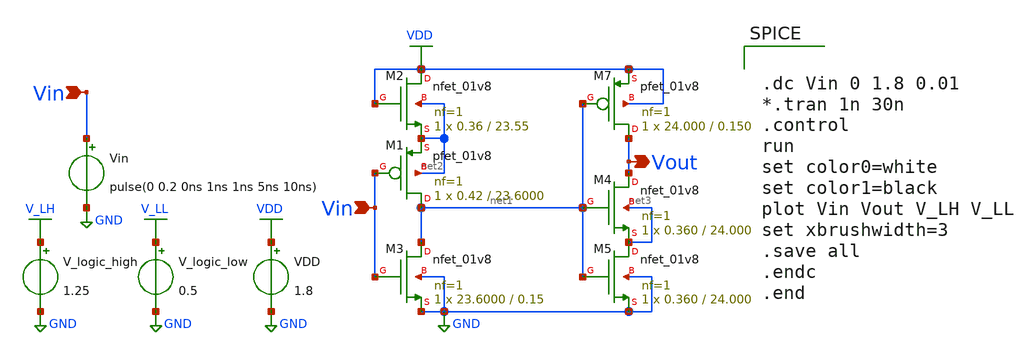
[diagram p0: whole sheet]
** sch_path: xschem/Vth_sch/th02.sch
**.subckt th02 Vin Vin Vout
*.ipin Vin
*.ipin Vin
*.opin Vout
VDD VDD GND 1.8
Vin Vin GND pulse(0 0.2 0ns 1ns 1ns 5ns 10ns)
V_logic_high V_LH GND 1.25
V_logic_low V_LL GND 0.5
XM7 Vout net1 VDD VDD sky130_fd_pr__pfet_01v8 L=0.150 W=24.000 nf=1 ad='int((nf+1)/2) * W/nf * 0.29'
+ as='int((nf+2)/2) * W/nf * 0.29' pd='2*int((nf+1)/2) * (W/nf + 0.29)' ps='2*int((nf+2)/2) * (W/nf + 0.29)'
+ nrd='0.29 / W' nrs='0.29 / W' sa=0 sb=0 sd=0 mult=1 m=1
XM1 net1 Vin net2 net2 sky130_fd_pr__pfet_01v8 L=23.6000 W=0.42 nf=1 ad='int((nf+1)/2) * W/nf * 0.29'
+ as='int((nf+2)/2) * W/nf * 0.29' pd='2*int((nf+1)/2) * (W/nf + 0.29)' ps='2*int((nf+2)/2) * (W/nf + 0.29)'
+ nrd='0.29 / W' nrs='0.29 / W' sa=0 sb=0 sd=0 mult=1 m=1
XM3 net1 Vin GND GND sky130_fd_pr__nfet_01v8 L=0.15 W=23.6000 nf=1 ad='int((nf+1)/2) * W/nf * 0.29' as='int((nf+2)/2) * W/nf * 0.29'
+ pd='2*int((nf+1)/2) * (W/nf + 0.29)' ps='2*int((nf+2)/2) * (W/nf + 0.29)' nrd='0.29 / W' nrs='0.29 / W'
+ sa=0 sb=0 sd=0 mult=1 m=1
XM2 VDD VDD net2 net2 sky130_fd_pr__nfet_01v8 L=23.55 W=0.36 nf=1 ad='int((nf+1)/2) * W/nf * 0.29' as='int((nf+2)/2) * W/nf * 0.29'
+ pd='2*int((nf+1)/2) * (W/nf + 0.29)' ps='2*int((nf+2)/2) * (W/nf + 0.29)' nrd='0.29 / W' nrs='0.29 / W'
+ sa=0 sb=0 sd=0 mult=1 m=1
XM4 Vout net1 net3 net3 sky130_fd_pr__nfet_01v8 L=24.000 W=0.360 nf=1 ad='int((nf+1)/2) * W/nf * 0.29'
+ as='int((nf+2)/2) * W/nf * 0.29' pd='2*int((nf+1)/2) * (W/nf + 0.29)' ps='2*int((nf+2)/2) * (W/nf + 0.29)'
+ nrd='0.29 / W' nrs='0.29 / W' sa=0 sb=0 sd=0 mult=1 m=1
XM5 net3 net1 GND GND sky130_fd_pr__nfet_01v8 L=24.000 W=0.360 nf=1 ad='int((nf+1)/2) * W/nf * 0.29'
+ as='int((nf+2)/2) * W/nf * 0.29' pd='2*int((nf+1)/2) * (W/nf + 0.29)' ps='2*int((nf+2)/2) * (W/nf + 0.29)'
+ nrd='0.29 / W' nrs='0.29 / W' sa=0 sb=0 sd=0 mult=1 m=1
**** begin user architecture code


.lib /usr/local/share/pdk/sky130A/libs.tech/ngspice/sky130.lib.spice tt

.save all





.dc Vin 0 1.8 0.01
*.tran 1n 30n
.control
run
set color0=white
set color1=black
plot Vin Vout V_LH V_LL
set xbrushwidth=3
.save all
.endc
.end


**** end user architecture code
**.ends
.GLOBAL VDD
.GLOBAL GND
.GLOBAL V_LH
.GLOBAL V_LL
.end
